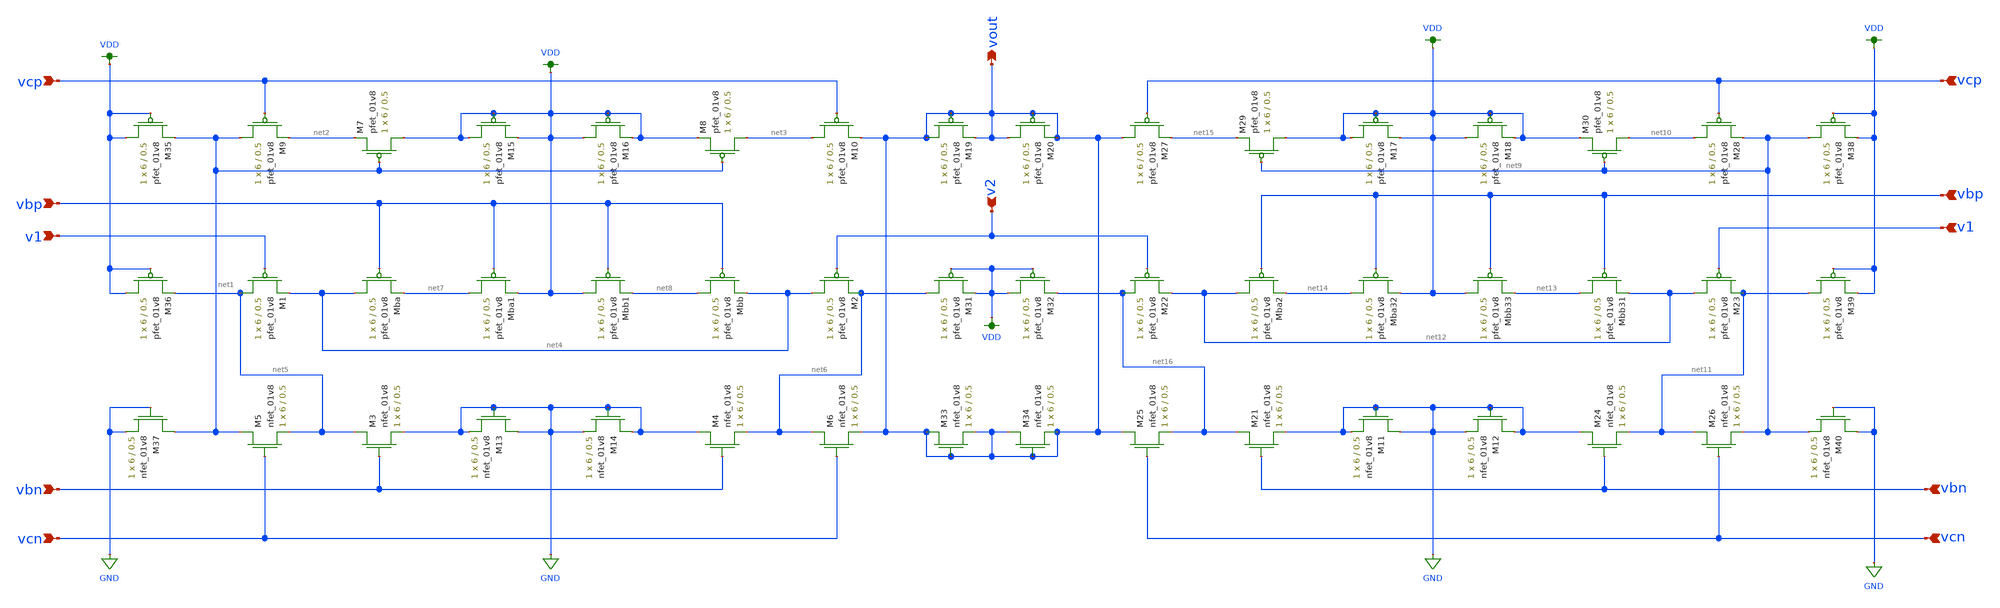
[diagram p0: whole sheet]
** sch_path: mini_proj_3/schematic/diff_amp_lvs.sch
**.subckt diff_amp_lvs vout v2 v1 v1 vbp vbp vcp vbn vcn vbn vcn vcp
*.opin vout
*.ipin v2
*.ipin v1
*.ipin v1
*.ipin vbp
*.ipin vbp
*.ipin vcp
*.ipin vbn
*.ipin vcn
*.ipin vbn
*.ipin vcn
*.ipin vcp
XMba net4 vbp net7 VDD sky130_fd_pr__pfet_01v8 L=0.5 W=6 nf=1 ad='int((nf+1)/2) * W/nf * 0.29' as='int((nf+2)/2) * W/nf * 0.29'
+ pd='2*int((nf+1)/2) * (W/nf + 0.29)' ps='2*int((nf+2)/2) * (W/nf + 0.29)' nrd='0.29 / W' nrs='0.29 / W'
+ sa=0 sb=0 sd=0 mult=1 m=1
XM3 net5 vbn GND GND sky130_fd_pr__nfet_01v8 L=0.5 W=6 nf=1 ad='int((nf+1)/2) * W/nf * 0.29' as='int((nf+2)/2) * W/nf * 0.29'
+ pd='2*int((nf+1)/2) * (W/nf + 0.29)' ps='2*int((nf+2)/2) * (W/nf + 0.29)' nrd='0.29 / W' nrs='0.29 / W'
+ sa=0 sb=0 sd=0 mult=1 m=1
XM1 net5 v1 net4 VDD sky130_fd_pr__pfet_01v8 L=0.5 W=6 nf=1 ad='int((nf+1)/2) * W/nf * 0.29' as='int((nf+2)/2) * W/nf * 0.29'
+ pd='2*int((nf+1)/2) * (W/nf + 0.29)' ps='2*int((nf+2)/2) * (W/nf + 0.29)' nrd='0.29 / W' nrs='0.29 / W'
+ sa=0 sb=0 sd=0 mult=1 m=1
XM2 net4 v2 net6 VDD sky130_fd_pr__pfet_01v8 L=0.5 W=6 nf=1 ad='int((nf+1)/2) * W/nf * 0.29' as='int((nf+2)/2) * W/nf * 0.29'
+ pd='2*int((nf+1)/2) * (W/nf + 0.29)' ps='2*int((nf+2)/2) * (W/nf + 0.29)' nrd='0.29 / W' nrs='0.29 / W'
+ sa=0 sb=0 sd=0 mult=1 m=1
XM4 GND vbn net6 GND sky130_fd_pr__nfet_01v8 L=0.5 W=6 nf=1 ad='int((nf+1)/2) * W/nf * 0.29' as='int((nf+2)/2) * W/nf * 0.29'
+ pd='2*int((nf+1)/2) * (W/nf + 0.29)' ps='2*int((nf+2)/2) * (W/nf + 0.29)' nrd='0.29 / W' nrs='0.29 / W'
+ sa=0 sb=0 sd=0 mult=1 m=1
XM5 net1 vcn net5 GND sky130_fd_pr__nfet_01v8 L=0.5 W=6 nf=1 ad='int((nf+1)/2) * W/nf * 0.29' as='int((nf+2)/2) * W/nf * 0.29'
+ pd='2*int((nf+1)/2) * (W/nf + 0.29)' ps='2*int((nf+2)/2) * (W/nf + 0.29)' nrd='0.29 / W' nrs='0.29 / W'
+ sa=0 sb=0 sd=0 mult=1 m=1
XM6 net6 vcn vout GND sky130_fd_pr__nfet_01v8 L=0.5 W=6 nf=1 ad='int((nf+1)/2) * W/nf * 0.29' as='int((nf+2)/2) * W/nf * 0.29'
+ pd='2*int((nf+1)/2) * (W/nf + 0.29)' ps='2*int((nf+2)/2) * (W/nf + 0.29)' nrd='0.29 / W' nrs='0.29 / W'
+ sa=0 sb=0 sd=0 mult=1 m=1
XM9 net1 vcp net2 VDD sky130_fd_pr__pfet_01v8 L=0.5 W=6 nf=1 ad='int((nf+1)/2) * W/nf * 0.29' as='int((nf+2)/2) * W/nf * 0.29'
+ pd='2*int((nf+1)/2) * (W/nf + 0.29)' ps='2*int((nf+2)/2) * (W/nf + 0.29)' nrd='0.29 / W' nrs='0.29 / W'
+ sa=0 sb=0 sd=0 mult=1 m=1
XM10 net3 vcp vout VDD sky130_fd_pr__pfet_01v8 L=0.5 W=6 nf=1 ad='int((nf+1)/2) * W/nf * 0.29' as='int((nf+2)/2) * W/nf * 0.29'
+ pd='2*int((nf+1)/2) * (W/nf + 0.29)' ps='2*int((nf+2)/2) * (W/nf + 0.29)' nrd='0.29 / W' nrs='0.29 / W'
+ sa=0 sb=0 sd=0 mult=1 m=1
XM7 VDD net1 net2 VDD sky130_fd_pr__pfet_01v8 L=0.5 W=6 nf=1 ad='int((nf+1)/2) * W/nf * 0.29' as='int((nf+2)/2) * W/nf * 0.29'
+ pd='2*int((nf+1)/2) * (W/nf + 0.29)' ps='2*int((nf+2)/2) * (W/nf + 0.29)' nrd='0.29 / W' nrs='0.29 / W'
+ sa=0 sb=0 sd=0 mult=1 m=1
XM8 net3 net1 VDD VDD sky130_fd_pr__pfet_01v8 L=0.5 W=6 nf=1 ad='int((nf+1)/2) * W/nf * 0.29' as='int((nf+2)/2) * W/nf * 0.29'
+ pd='2*int((nf+1)/2) * (W/nf + 0.29)' ps='2*int((nf+2)/2) * (W/nf + 0.29)' nrd='0.29 / W' nrs='0.29 / W'
+ sa=0 sb=0 sd=0 mult=1 m=1
XMbb net8 vbp net4 VDD sky130_fd_pr__pfet_01v8 L=0.5 W=6 nf=1 ad='int((nf+1)/2) * W/nf * 0.29' as='int((nf+2)/2) * W/nf * 0.29'
+ pd='2*int((nf+1)/2) * (W/nf + 0.29)' ps='2*int((nf+2)/2) * (W/nf + 0.29)' nrd='0.29 / W' nrs='0.29 / W'
+ sa=0 sb=0 sd=0 mult=1 m=1
XMba1 net7 vbp VDD VDD sky130_fd_pr__pfet_01v8 L=0.5 W=6 nf=1 ad='int((nf+1)/2) * W/nf * 0.29' as='int((nf+2)/2) * W/nf * 0.29'
+ pd='2*int((nf+1)/2) * (W/nf + 0.29)' ps='2*int((nf+2)/2) * (W/nf + 0.29)' nrd='0.29 / W' nrs='0.29 / W'
+ sa=0 sb=0 sd=0 mult=1 m=1
XMbb1 VDD vbp net8 VDD sky130_fd_pr__pfet_01v8 L=0.5 W=6 nf=1 ad='int((nf+1)/2) * W/nf * 0.29' as='int((nf+2)/2) * W/nf * 0.29'
+ pd='2*int((nf+1)/2) * (W/nf + 0.29)' ps='2*int((nf+2)/2) * (W/nf + 0.29)' nrd='0.29 / W' nrs='0.29 / W'
+ sa=0 sb=0 sd=0 mult=1 m=1
XMba2 net12 vbp net14 VDD sky130_fd_pr__pfet_01v8 L=0.5 W=6 nf=1 ad='int((nf+1)/2) * W/nf * 0.29' as='int((nf+2)/2) * W/nf * 0.29'
+ pd='2*int((nf+1)/2) * (W/nf + 0.29)' ps='2*int((nf+2)/2) * (W/nf + 0.29)' nrd='0.29 / W' nrs='0.29 / W'
+ sa=0 sb=0 sd=0 mult=1 m=1
XM21 net16 vbn GND GND sky130_fd_pr__nfet_01v8 L=0.5 W=6 nf=1 ad='int((nf+1)/2) * W/nf * 0.29' as='int((nf+2)/2) * W/nf * 0.29'
+ pd='2*int((nf+1)/2) * (W/nf + 0.29)' ps='2*int((nf+2)/2) * (W/nf + 0.29)' nrd='0.29 / W' nrs='0.29 / W'
+ sa=0 sb=0 sd=0 mult=1 m=1
XM22 net16 v2 net12 VDD sky130_fd_pr__pfet_01v8 L=0.5 W=6 nf=1 ad='int((nf+1)/2) * W/nf * 0.29' as='int((nf+2)/2) * W/nf * 0.29'
+ pd='2*int((nf+1)/2) * (W/nf + 0.29)' ps='2*int((nf+2)/2) * (W/nf + 0.29)' nrd='0.29 / W' nrs='0.29 / W'
+ sa=0 sb=0 sd=0 mult=1 m=1
XM23 net12 v1 net11 VDD sky130_fd_pr__pfet_01v8 L=0.5 W=6 nf=1 ad='int((nf+1)/2) * W/nf * 0.29' as='int((nf+2)/2) * W/nf * 0.29'
+ pd='2*int((nf+1)/2) * (W/nf + 0.29)' ps='2*int((nf+2)/2) * (W/nf + 0.29)' nrd='0.29 / W' nrs='0.29 / W'
+ sa=0 sb=0 sd=0 mult=1 m=1
XM24 GND vbn net11 GND sky130_fd_pr__nfet_01v8 L=0.5 W=6 nf=1 ad='int((nf+1)/2) * W/nf * 0.29' as='int((nf+2)/2) * W/nf * 0.29'
+ pd='2*int((nf+1)/2) * (W/nf + 0.29)' ps='2*int((nf+2)/2) * (W/nf + 0.29)' nrd='0.29 / W' nrs='0.29 / W'
+ sa=0 sb=0 sd=0 mult=1 m=1
XM25 vout vcn net16 GND sky130_fd_pr__nfet_01v8 L=0.5 W=6 nf=1 ad='int((nf+1)/2) * W/nf * 0.29' as='int((nf+2)/2) * W/nf * 0.29'
+ pd='2*int((nf+1)/2) * (W/nf + 0.29)' ps='2*int((nf+2)/2) * (W/nf + 0.29)' nrd='0.29 / W' nrs='0.29 / W'
+ sa=0 sb=0 sd=0 mult=1 m=1
XM26 net11 vcn net9 GND sky130_fd_pr__nfet_01v8 L=0.5 W=6 nf=1 ad='int((nf+1)/2) * W/nf * 0.29' as='int((nf+2)/2) * W/nf * 0.29'
+ pd='2*int((nf+1)/2) * (W/nf + 0.29)' ps='2*int((nf+2)/2) * (W/nf + 0.29)' nrd='0.29 / W' nrs='0.29 / W'
+ sa=0 sb=0 sd=0 mult=1 m=1
XM27 vout vcp net15 VDD sky130_fd_pr__pfet_01v8 L=0.5 W=6 nf=1 ad='int((nf+1)/2) * W/nf * 0.29' as='int((nf+2)/2) * W/nf * 0.29'
+ pd='2*int((nf+1)/2) * (W/nf + 0.29)' ps='2*int((nf+2)/2) * (W/nf + 0.29)' nrd='0.29 / W' nrs='0.29 / W'
+ sa=0 sb=0 sd=0 mult=1 m=1
XM28 net10 vcp net9 VDD sky130_fd_pr__pfet_01v8 L=0.5 W=6 nf=1 ad='int((nf+1)/2) * W/nf * 0.29' as='int((nf+2)/2) * W/nf * 0.29'
+ pd='2*int((nf+1)/2) * (W/nf + 0.29)' ps='2*int((nf+2)/2) * (W/nf + 0.29)' nrd='0.29 / W' nrs='0.29 / W'
+ sa=0 sb=0 sd=0 mult=1 m=1
XM29 VDD net9 net15 VDD sky130_fd_pr__pfet_01v8 L=0.5 W=6 nf=1 ad='int((nf+1)/2) * W/nf * 0.29' as='int((nf+2)/2) * W/nf * 0.29'
+ pd='2*int((nf+1)/2) * (W/nf + 0.29)' ps='2*int((nf+2)/2) * (W/nf + 0.29)' nrd='0.29 / W' nrs='0.29 / W'
+ sa=0 sb=0 sd=0 mult=1 m=1
XM30 net10 net9 VDD VDD sky130_fd_pr__pfet_01v8 L=0.5 W=6 nf=1 ad='int((nf+1)/2) * W/nf * 0.29' as='int((nf+2)/2) * W/nf * 0.29'
+ pd='2*int((nf+1)/2) * (W/nf + 0.29)' ps='2*int((nf+2)/2) * (W/nf + 0.29)' nrd='0.29 / W' nrs='0.29 / W'
+ sa=0 sb=0 sd=0 mult=1 m=1
XMbb31 net13 vbp net12 VDD sky130_fd_pr__pfet_01v8 L=0.5 W=6 nf=1 ad='int((nf+1)/2) * W/nf * 0.29' as='int((nf+2)/2) * W/nf * 0.29'
+ pd='2*int((nf+1)/2) * (W/nf + 0.29)' ps='2*int((nf+2)/2) * (W/nf + 0.29)' nrd='0.29 / W' nrs='0.29 / W'
+ sa=0 sb=0 sd=0 mult=1 m=1
XMba32 net14 vbp VDD VDD sky130_fd_pr__pfet_01v8 L=0.5 W=6 nf=1 ad='int((nf+1)/2) * W/nf * 0.29' as='int((nf+2)/2) * W/nf * 0.29'
+ pd='2*int((nf+1)/2) * (W/nf + 0.29)' ps='2*int((nf+2)/2) * (W/nf + 0.29)' nrd='0.29 / W' nrs='0.29 / W'
+ sa=0 sb=0 sd=0 mult=1 m=1
XMbb33 VDD vbp net13 VDD sky130_fd_pr__pfet_01v8 L=0.5 W=6 nf=1 ad='int((nf+1)/2) * W/nf * 0.29' as='int((nf+2)/2) * W/nf * 0.29'
+ pd='2*int((nf+1)/2) * (W/nf + 0.29)' ps='2*int((nf+2)/2) * (W/nf + 0.29)' nrd='0.29 / W' nrs='0.29 / W'
+ sa=0 sb=0 sd=0 mult=1 m=1
XM11 GND GND GND GND sky130_fd_pr__nfet_01v8 L=0.5 W=6 nf=1 ad='int((nf+1)/2) * W/nf * 0.29' as='int((nf+2)/2) * W/nf * 0.29'
+ pd='2*int((nf+1)/2) * (W/nf + 0.29)' ps='2*int((nf+2)/2) * (W/nf + 0.29)' nrd='0.29 / W' nrs='0.29 / W'
+ sa=0 sb=0 sd=0 mult=1 m=1
XM12 GND GND GND GND sky130_fd_pr__nfet_01v8 L=0.5 W=6 nf=1 ad='int((nf+1)/2) * W/nf * 0.29' as='int((nf+2)/2) * W/nf * 0.29'
+ pd='2*int((nf+1)/2) * (W/nf + 0.29)' ps='2*int((nf+2)/2) * (W/nf + 0.29)' nrd='0.29 / W' nrs='0.29 / W'
+ sa=0 sb=0 sd=0 mult=1 m=1
XM13 GND GND GND GND sky130_fd_pr__nfet_01v8 L=0.5 W=6 nf=1 ad='int((nf+1)/2) * W/nf * 0.29' as='int((nf+2)/2) * W/nf * 0.29'
+ pd='2*int((nf+1)/2) * (W/nf + 0.29)' ps='2*int((nf+2)/2) * (W/nf + 0.29)' nrd='0.29 / W' nrs='0.29 / W'
+ sa=0 sb=0 sd=0 mult=1 m=1
XM14 GND GND GND GND sky130_fd_pr__nfet_01v8 L=0.5 W=6 nf=1 ad='int((nf+1)/2) * W/nf * 0.29' as='int((nf+2)/2) * W/nf * 0.29'
+ pd='2*int((nf+1)/2) * (W/nf + 0.29)' ps='2*int((nf+2)/2) * (W/nf + 0.29)' nrd='0.29 / W' nrs='0.29 / W'
+ sa=0 sb=0 sd=0 mult=1 m=1
XM15 VDD VDD VDD VDD sky130_fd_pr__pfet_01v8 L=0.5 W=6 nf=1 ad='int((nf+1)/2) * W/nf * 0.29' as='int((nf+2)/2) * W/nf * 0.29'
+ pd='2*int((nf+1)/2) * (W/nf + 0.29)' ps='2*int((nf+2)/2) * (W/nf + 0.29)' nrd='0.29 / W' nrs='0.29 / W'
+ sa=0 sb=0 sd=0 mult=1 m=1
XM16 VDD VDD VDD VDD sky130_fd_pr__pfet_01v8 L=0.5 W=6 nf=1 ad='int((nf+1)/2) * W/nf * 0.29' as='int((nf+2)/2) * W/nf * 0.29'
+ pd='2*int((nf+1)/2) * (W/nf + 0.29)' ps='2*int((nf+2)/2) * (W/nf + 0.29)' nrd='0.29 / W' nrs='0.29 / W'
+ sa=0 sb=0 sd=0 mult=1 m=1
XM17 VDD VDD VDD VDD sky130_fd_pr__pfet_01v8 L=0.5 W=6 nf=1 ad='int((nf+1)/2) * W/nf * 0.29' as='int((nf+2)/2) * W/nf * 0.29'
+ pd='2*int((nf+1)/2) * (W/nf + 0.29)' ps='2*int((nf+2)/2) * (W/nf + 0.29)' nrd='0.29 / W' nrs='0.29 / W'
+ sa=0 sb=0 sd=0 mult=1 m=1
XM18 VDD VDD VDD VDD sky130_fd_pr__pfet_01v8 L=0.5 W=6 nf=1 ad='int((nf+1)/2) * W/nf * 0.29' as='int((nf+2)/2) * W/nf * 0.29'
+ pd='2*int((nf+1)/2) * (W/nf + 0.29)' ps='2*int((nf+2)/2) * (W/nf + 0.29)' nrd='0.29 / W' nrs='0.29 / W'
+ sa=0 sb=0 sd=0 mult=1 m=1
XM19 vout vout vout VDD sky130_fd_pr__pfet_01v8 L=0.5 W=6 nf=1 ad='int((nf+1)/2) * W/nf * 0.29' as='int((nf+2)/2) * W/nf * 0.29'
+ pd='2*int((nf+1)/2) * (W/nf + 0.29)' ps='2*int((nf+2)/2) * (W/nf + 0.29)' nrd='0.29 / W' nrs='0.29 / W'
+ sa=0 sb=0 sd=0 mult=1 m=1
XM20 vout vout vout VDD sky130_fd_pr__pfet_01v8 L=0.5 W=6 nf=1 ad='int((nf+1)/2) * W/nf * 0.29' as='int((nf+2)/2) * W/nf * 0.29'
+ pd='2*int((nf+1)/2) * (W/nf + 0.29)' ps='2*int((nf+2)/2) * (W/nf + 0.29)' nrd='0.29 / W' nrs='0.29 / W'
+ sa=0 sb=0 sd=0 mult=1 m=1
XM31 net6 VDD VDD VDD sky130_fd_pr__pfet_01v8 L=0.5 W=6 nf=1 ad='int((nf+1)/2) * W/nf * 0.29' as='int((nf+2)/2) * W/nf * 0.29'
+ pd='2*int((nf+1)/2) * (W/nf + 0.29)' ps='2*int((nf+2)/2) * (W/nf + 0.29)' nrd='0.29 / W' nrs='0.29 / W'
+ sa=0 sb=0 sd=0 mult=1 m=1
XM32 VDD VDD net16 VDD sky130_fd_pr__pfet_01v8 L=0.5 W=6 nf=1 ad='int((nf+1)/2) * W/nf * 0.29' as='int((nf+2)/2) * W/nf * 0.29'
+ pd='2*int((nf+1)/2) * (W/nf + 0.29)' ps='2*int((nf+2)/2) * (W/nf + 0.29)' nrd='0.29 / W' nrs='0.29 / W'
+ sa=0 sb=0 sd=0 mult=1 m=1
XM35 VDD VDD net1 VDD sky130_fd_pr__pfet_01v8 L=0.5 W=6 nf=1 ad='int((nf+1)/2) * W/nf * 0.29' as='int((nf+2)/2) * W/nf * 0.29'
+ pd='2*int((nf+1)/2) * (W/nf + 0.29)' ps='2*int((nf+2)/2) * (W/nf + 0.29)' nrd='0.29 / W' nrs='0.29 / W'
+ sa=0 sb=0 sd=0 mult=1 m=1
XM36 VDD VDD net5 VDD sky130_fd_pr__pfet_01v8 L=0.5 W=6 nf=1 ad='int((nf+1)/2) * W/nf * 0.29' as='int((nf+2)/2) * W/nf * 0.29'
+ pd='2*int((nf+1)/2) * (W/nf + 0.29)' ps='2*int((nf+2)/2) * (W/nf + 0.29)' nrd='0.29 / W' nrs='0.29 / W'
+ sa=0 sb=0 sd=0 mult=1 m=1
XM33 vout vout vout GND sky130_fd_pr__nfet_01v8 L=0.5 W=6 nf=1 ad='int((nf+1)/2) * W/nf * 0.29' as='int((nf+2)/2) * W/nf * 0.29'
+ pd='2*int((nf+1)/2) * (W/nf + 0.29)' ps='2*int((nf+2)/2) * (W/nf + 0.29)' nrd='0.29 / W' nrs='0.29 / W'
+ sa=0 sb=0 sd=0 mult=1 m=1
XM34 vout vout vout GND sky130_fd_pr__nfet_01v8 L=0.5 W=6 nf=1 ad='int((nf+1)/2) * W/nf * 0.29' as='int((nf+2)/2) * W/nf * 0.29'
+ pd='2*int((nf+1)/2) * (W/nf + 0.29)' ps='2*int((nf+2)/2) * (W/nf + 0.29)' nrd='0.29 / W' nrs='0.29 / W'
+ sa=0 sb=0 sd=0 mult=1 m=1
XM37 net1 GND GND GND sky130_fd_pr__nfet_01v8 L=0.5 W=6 nf=1 ad='int((nf+1)/2) * W/nf * 0.29' as='int((nf+2)/2) * W/nf * 0.29'
+ pd='2*int((nf+1)/2) * (W/nf + 0.29)' ps='2*int((nf+2)/2) * (W/nf + 0.29)' nrd='0.29 / W' nrs='0.29 / W'
+ sa=0 sb=0 sd=0 mult=1 m=1
XM38 net9 VDD VDD VDD sky130_fd_pr__pfet_01v8 L=0.5 W=6 nf=1 ad='int((nf+1)/2) * W/nf * 0.29' as='int((nf+2)/2) * W/nf * 0.29'
+ pd='2*int((nf+1)/2) * (W/nf + 0.29)' ps='2*int((nf+2)/2) * (W/nf + 0.29)' nrd='0.29 / W' nrs='0.29 / W'
+ sa=0 sb=0 sd=0 mult=1 m=1
XM39 net11 VDD VDD VDD sky130_fd_pr__pfet_01v8 L=0.5 W=6 nf=1 ad='int((nf+1)/2) * W/nf * 0.29' as='int((nf+2)/2) * W/nf * 0.29'
+ pd='2*int((nf+1)/2) * (W/nf + 0.29)' ps='2*int((nf+2)/2) * (W/nf + 0.29)' nrd='0.29 / W' nrs='0.29 / W'
+ sa=0 sb=0 sd=0 mult=1 m=1
XM40 GND GND net9 GND sky130_fd_pr__nfet_01v8 L=0.5 W=6 nf=1 ad='int((nf+1)/2) * W/nf * 0.29' as='int((nf+2)/2) * W/nf * 0.29'
+ pd='2*int((nf+1)/2) * (W/nf + 0.29)' ps='2*int((nf+2)/2) * (W/nf + 0.29)' nrd='0.29 / W' nrs='0.29 / W'
+ sa=0 sb=0 sd=0 mult=1 m=1
**.ends
.GLOBAL GND
.GLOBAL VDD
.end
